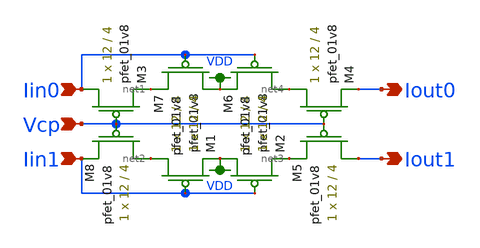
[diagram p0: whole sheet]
** sch_path: modules/cascode_mirror_lds.sch
**.subckt cascode_mirror_lds Vcp Iin0 Iout0 Iin1 Iout1
*.ipin Vcp
*.ipin Iin0
*.opin Iout0
*.ipin Iin1
*.opin Iout1
XM3 Iin0 Vcp net1 VDD sky130_fd_pr__pfet_01v8 L=4 W=12 nf=1 ad='int((nf+1)/2) * W/nf * 0.29' as='int((nf+2)/2) * W/nf * 0.29'
+ pd='2*int((nf+1)/2) * (W/nf + 0.29)' ps='2*int((nf+2)/2) * (W/nf + 0.29)' nrd='0.29 / W' nrs='0.29 / W'
+ sa=0 sb=0 sd=0 mult=1 m=1
XM1 net2 Iin1 VDD VDD sky130_fd_pr__pfet_01v8 L=4 W=12 nf=1 ad='int((nf+1)/2) * W/nf * 0.29' as='int((nf+2)/2) * W/nf * 0.29'
+ pd='2*int((nf+1)/2) * (W/nf + 0.29)' ps='2*int((nf+2)/2) * (W/nf + 0.29)' nrd='0.29 / W' nrs='0.29 / W'
+ sa=0 sb=0 sd=0 mult=1 m=1
XM2 VDD Iin1 net3 VDD sky130_fd_pr__pfet_01v8 L=4 W=12 nf=1 ad='int((nf+1)/2) * W/nf * 0.29' as='int((nf+2)/2) * W/nf * 0.29'
+ pd='2*int((nf+1)/2) * (W/nf + 0.29)' ps='2*int((nf+2)/2) * (W/nf + 0.29)' nrd='0.29 / W' nrs='0.29 / W'
+ sa=0 sb=0 sd=0 mult=1 m=1
XM4 net4 Vcp Iout0 VDD sky130_fd_pr__pfet_01v8 L=4 W=12 nf=1 ad='int((nf+1)/2) * W/nf * 0.29' as='int((nf+2)/2) * W/nf * 0.29'
+ pd='2*int((nf+1)/2) * (W/nf + 0.29)' ps='2*int((nf+2)/2) * (W/nf + 0.29)' nrd='0.29 / W' nrs='0.29 / W'
+ sa=0 sb=0 sd=0 mult=1 m=1
XM5 Iout1 Vcp net3 VDD sky130_fd_pr__pfet_01v8 L=4 W=12 nf=1 ad='int((nf+1)/2) * W/nf * 0.29' as='int((nf+2)/2) * W/nf * 0.29'
+ pd='2*int((nf+1)/2) * (W/nf + 0.29)' ps='2*int((nf+2)/2) * (W/nf + 0.29)' nrd='0.29 / W' nrs='0.29 / W'
+ sa=0 sb=0 sd=0 mult=1 m=1
XM6 net4 Iin0 VDD VDD sky130_fd_pr__pfet_01v8 L=4 W=12 nf=1 ad='int((nf+1)/2) * W/nf * 0.29' as='int((nf+2)/2) * W/nf * 0.29'
+ pd='2*int((nf+1)/2) * (W/nf + 0.29)' ps='2*int((nf+2)/2) * (W/nf + 0.29)' nrd='0.29 / W' nrs='0.29 / W'
+ sa=0 sb=0 sd=0 mult=1 m=1
XM7 VDD Iin0 net1 VDD sky130_fd_pr__pfet_01v8 L=4 W=12 nf=1 ad='int((nf+1)/2) * W/nf * 0.29' as='int((nf+2)/2) * W/nf * 0.29'
+ pd='2*int((nf+1)/2) * (W/nf + 0.29)' ps='2*int((nf+2)/2) * (W/nf + 0.29)' nrd='0.29 / W' nrs='0.29 / W'
+ sa=0 sb=0 sd=0 mult=1 m=1
XM8 net2 Vcp Iin1 VDD sky130_fd_pr__pfet_01v8 L=4 W=12 nf=1 ad='int((nf+1)/2) * W/nf * 0.29' as='int((nf+2)/2) * W/nf * 0.29'
+ pd='2*int((nf+1)/2) * (W/nf + 0.29)' ps='2*int((nf+2)/2) * (W/nf + 0.29)' nrd='0.29 / W' nrs='0.29 / W'
+ sa=0 sb=0 sd=0 mult=1 m=1
**.ends
.GLOBAL VDD
.end
